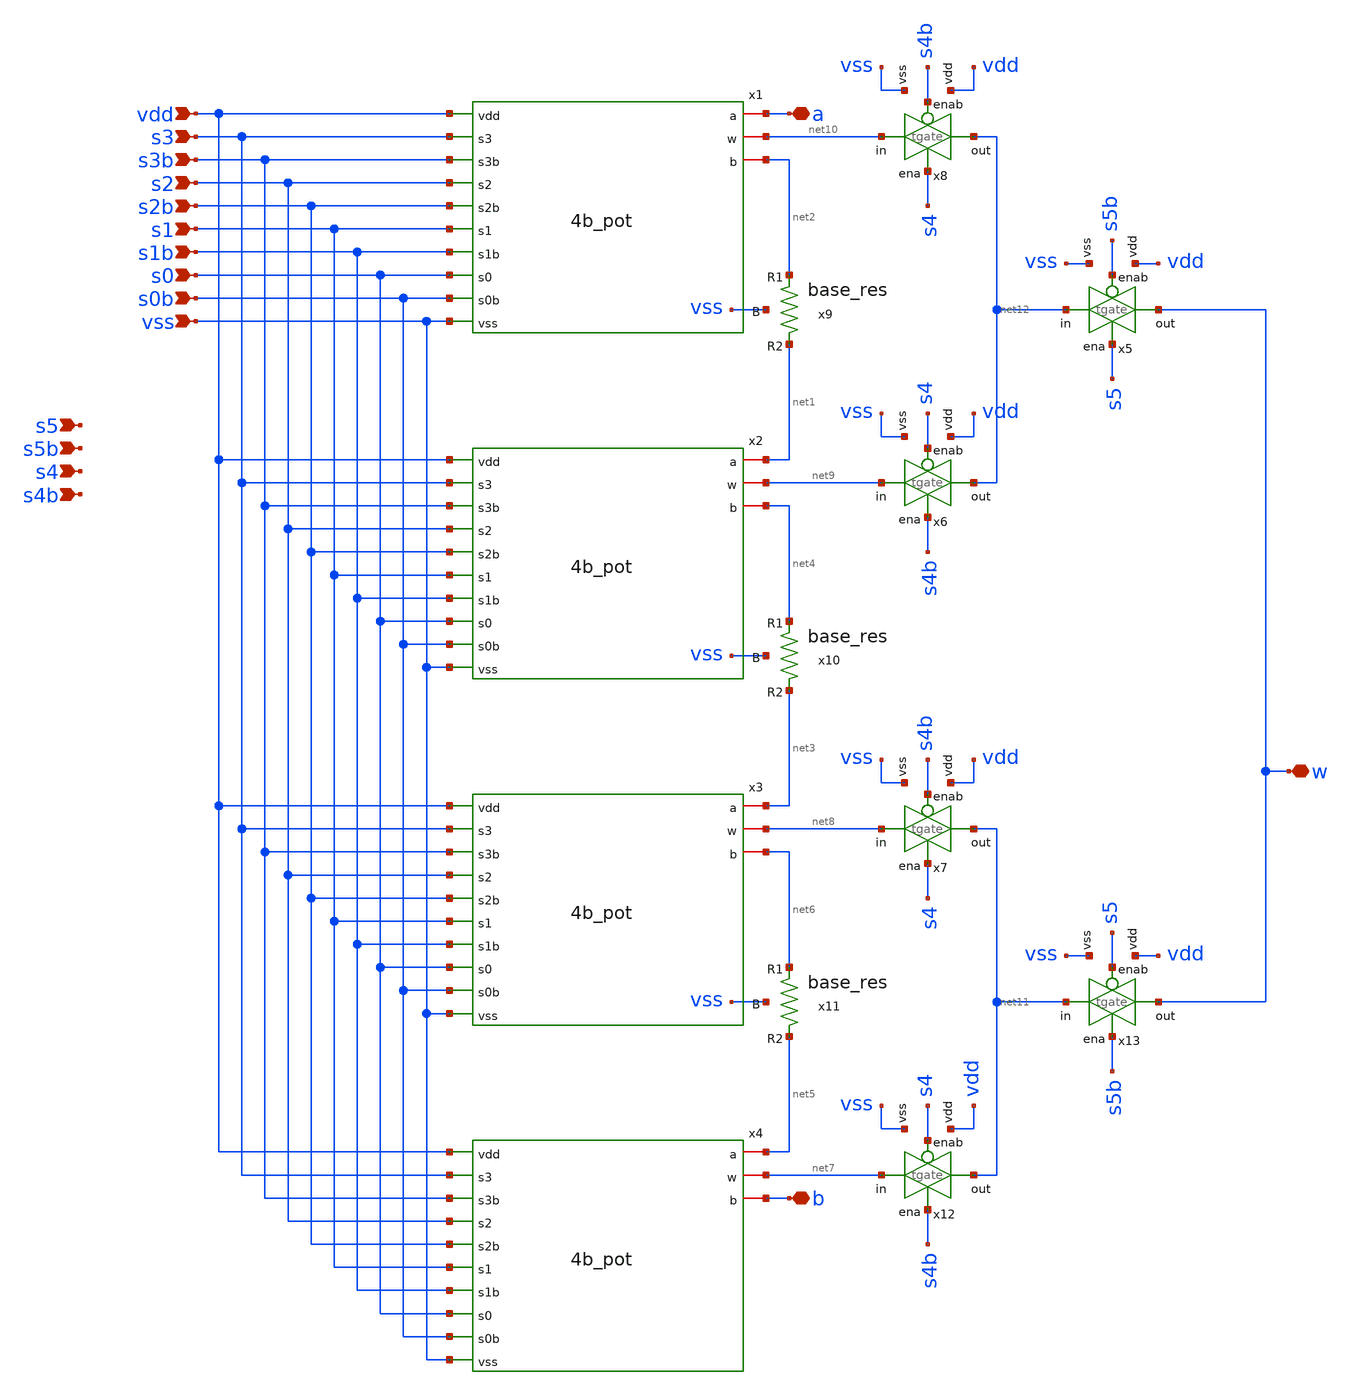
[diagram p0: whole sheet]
** sch_path: xschem/6b_pot.sch
**.subckt 6b_pot s0 s0b s1 s1b s2 s2b s3 s3b s4 s4b s5 s5b vss vdd a w b
*.ipin s0
*.ipin s0b
*.ipin s1
*.ipin s1b
*.ipin s2
*.ipin s2b
*.ipin s3
*.ipin s3b
*.ipin s4
*.ipin s4b
*.ipin s5
*.ipin s5b
*.ipin vss
*.ipin vdd
*.iopin a
*.iopin w
*.iopin b
x1 vdd a s3 s3b s2 s2b net10 s1 s1b s0 s0b net2 vss 4b_pot
x2 vdd net1 s3 s3b s2 s2b net9 s1 s1b s0 s0b net4 vss 4b_pot
x3 vdd net3 s3 s3b s2 s2b net8 s1 s1b s0 s0b net6 vss 4b_pot
x4 vdd net5 s3 s3b s2 s2b net7 s1 s1b s0 s0b b vss 4b_pot
x9 net2 net1 vss base_res
x10 net4 net3 vss base_res
x11 net6 net5 vss base_res
x8 vdd s4b net10 net12 s4 vss tgate
x5 vdd s5b net12 w s5 vss tgate
x6 vdd s4 net9 net12 s4b vss tgate
x7 vdd s4b net8 net11 s4 vss tgate
x12 vdd s4 net7 net11 s4b vss tgate
x13 vdd s5 net11 w s5b vss tgate
**.ends

* expanding   symbol:  xschem/4b_pot.sym # of pins=13
** sym_path: xschem/4b_pot.sym
** sch_path: xschem/4b_pot.sch
.subckt 4b_pot vdd a s3 s3b s2 s2b w s1 s1b s0 s0b b vss
*.ipin s0
*.ipin s0b
*.ipin s1
*.ipin s1b
*.ipin s2
*.ipin s2b
*.ipin s3
*.ipin s3b
*.ipin vss
*.ipin vdd
*.iopin a
*.iopin w
*.iopin b
x9 net7 net8 vss base_res
x1 vdd a s1 s1b net4 s0 s0b net7 vss 2b_pot
x2 vdd net8 s1 s1b net3 s0 s0b net9 vss 2b_pot
x3 vdd net10 s1 s1b net2 s0 s0b net11 vss 2b_pot
x4 vdd net12 s1 s1b net1 s0 s0b b vss 2b_pot
x5 net9 net10 vss base_res
x6 net11 net12 vss base_res
x8 vdd s2b net4 net6 s2 vss tgate
x7 vdd s2 net3 net6 s2b vss tgate
x10 vdd s2b net2 net5 s2 vss tgate
x11 vdd s2 net1 net5 s2b vss tgate
x12 vdd s3 net5 w s3b vss tgate
x13 vdd s3b net6 w s3 vss tgate
.ends


* expanding   symbol:  xschem/base_res.sym # of pins=3
** sym_path: xschem/base_res.sym
** sch_path: xschem/base_res.sch
.subckt base_res R1 R2 B
*.iopin R1
*.iopin R2
*.iopin B
XR2 R2 R1 B sky130_fd_pr__res_high_po_2p85 L=0.57 mult=1 m=1
.ends


* expanding   symbol:  xschem/tgate.sym # of pins=6
** sym_path: xschem/tgate.sym
** sch_path: xschem/tgate.sch
.subckt tgate vdd enab in out ena vss
*.ipin enab
*.ipin ena
*.ipin in
*.opin out
*.iopin vdd
*.iopin vss
XMn out ena in vss sky130_fd_pr__nfet_g5v0d10v5 L=0.5 W=80 nf=4 ad='int((nf+1)/2) * W/nf * 0.29' as='int((nf+2)/2) * W/nf * 0.29'
+ pd='2*int((nf+1)/2) * (W/nf + 0.29)' ps='2*int((nf+2)/2) * (W/nf + 0.29)' nrd='0.29 / W' nrs='0.29 / W'
+ sa=0 sb=0 sd=0 mult=1 m=1
XMp out enab in vdd sky130_fd_pr__pfet_g5v0d10v5 L=0.5 W=80 nf=4 ad='int((nf+1)/2) * W/nf * 0.29' as='int((nf+2)/2) * W/nf * 0.29'
+ pd='2*int((nf+1)/2) * (W/nf + 0.29)' ps='2*int((nf+2)/2) * (W/nf + 0.29)' nrd='0.29 / W' nrs='0.29 / W'
+ sa=0 sb=0 sd=0 mult=1 m=1
.ends


* expanding   symbol:  xschem/2b_pot.sym # of pins=9
** sym_path: xschem/2b_pot.sym
** sch_path: xschem/2b_pot.sch
.subckt 2b_pot vdd a s1 s1b w s0 s0b b vss
*.ipin s0
*.ipin s0b
*.ipin s1
*.ipin vss
*.ipin vdd
*.iopin a
*.iopin w
*.iopin b
*.ipin s1b
x1 vdd a net4 s0b s0 net1 vss 1b_pot
x2 vdd net2 net3 s0b s0 b vss 1b_pot
x5 net1 net2 vss base_res
x8 vdd s1b net4 w s1 vss tgate
x3 vdd s1 net3 w s1b vss tgate
.ends


* expanding   symbol:  xschem/1b_pot.sym # of pins=7
** sym_path: xschem/1b_pot.sym
** sch_path: xschem/1b_pot.sch
.subckt 1b_pot vdd a w s0b s0 b vss
*.ipin s0
*.ipin s0b
*.ipin vdd
*.ipin vss
*.ipin a
*.ipin b
*.opin w
x1 a b vss base_res
x2 vdd s0b a w s0 vss tgate
x3 vdd s0 b w s0b vss tgate
.ends

.end
